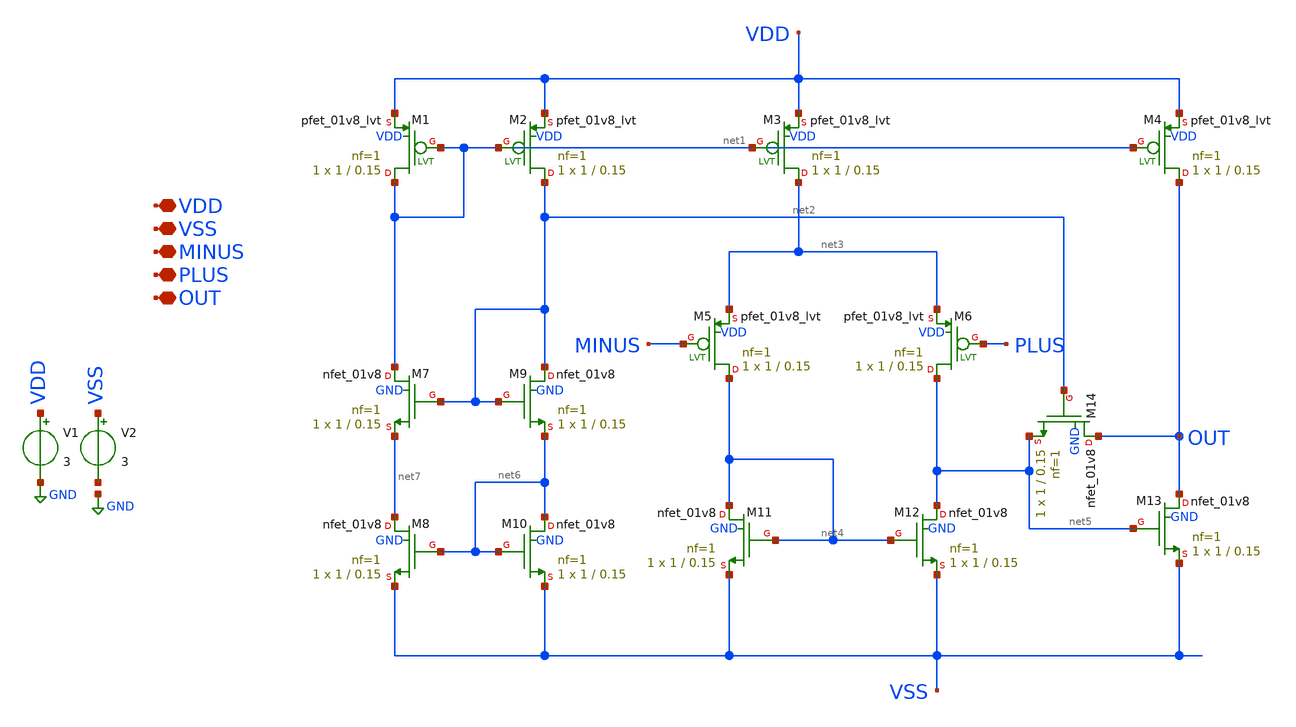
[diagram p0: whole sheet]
** sch_path: peak_two/peak_two.sch
**.subckt peak_two VDD VSS MINUS PLUS OUT
*.iopin VDD
*.iopin VSS
*.iopin MINUS
*.iopin PLUS
*.iopin OUT
XM1 net1 net1 VDD VDD sky130_fd_pr__pfet_01v8_lvt L=0.15 W=1 nf=1 ad='int((nf+1)/2) * W/nf * 0.29' as='int((nf+2)/2) * W/nf * 0.29'
+ pd='2*int((nf+1)/2) * (W/nf + 0.29)' ps='2*int((nf+2)/2) * (W/nf + 0.29)' nrd='0.29 / W' nrs='0.29 / W'
+ sa=0 sb=0 sd=0 mult=1 m=1
XM2 net2 net1 VDD VDD sky130_fd_pr__pfet_01v8_lvt L=0.15 W=1 nf=1 ad='int((nf+1)/2) * W/nf * 0.29' as='int((nf+2)/2) * W/nf * 0.29'
+ pd='2*int((nf+1)/2) * (W/nf + 0.29)' ps='2*int((nf+2)/2) * (W/nf + 0.29)' nrd='0.29 / W' nrs='0.29 / W'
+ sa=0 sb=0 sd=0 mult=1 m=1
XM3 net3 net1 VDD VDD sky130_fd_pr__pfet_01v8_lvt L=0.15 W=1 nf=1 ad='int((nf+1)/2) * W/nf * 0.29' as='int((nf+2)/2) * W/nf * 0.29'
+ pd='2*int((nf+1)/2) * (W/nf + 0.29)' ps='2*int((nf+2)/2) * (W/nf + 0.29)' nrd='0.29 / W' nrs='0.29 / W'
+ sa=0 sb=0 sd=0 mult=1 m=1
XM4 OUT net1 VDD VDD sky130_fd_pr__pfet_01v8_lvt L=0.15 W=1 nf=1 ad='int((nf+1)/2) * W/nf * 0.29' as='int((nf+2)/2) * W/nf * 0.29'
+ pd='2*int((nf+1)/2) * (W/nf + 0.29)' ps='2*int((nf+2)/2) * (W/nf + 0.29)' nrd='0.29 / W' nrs='0.29 / W'
+ sa=0 sb=0 sd=0 mult=1 m=1
XM5 net4 MINUS net3 VDD sky130_fd_pr__pfet_01v8_lvt L=0.15 W=1 nf=1 ad='int((nf+1)/2) * W/nf * 0.29'
+ as='int((nf+2)/2) * W/nf * 0.29' pd='2*int((nf+1)/2) * (W/nf + 0.29)' ps='2*int((nf+2)/2) * (W/nf + 0.29)'
+ nrd='0.29 / W' nrs='0.29 / W' sa=0 sb=0 sd=0 mult=1 m=1
XM6 net5 PLUS net3 VDD sky130_fd_pr__pfet_01v8_lvt L=0.15 W=1 nf=1 ad='int((nf+1)/2) * W/nf * 0.29' as='int((nf+2)/2) * W/nf * 0.29'
+ pd='2*int((nf+1)/2) * (W/nf + 0.29)' ps='2*int((nf+2)/2) * (W/nf + 0.29)' nrd='0.29 / W' nrs='0.29 / W'
+ sa=0 sb=0 sd=0 mult=1 m=1
XM9 net2 net2 net6 GND sky130_fd_pr__nfet_01v8 L=0.15 W=1 nf=1 ad='int((nf+1)/2) * W/nf * 0.29' as='int((nf+2)/2) * W/nf * 0.29'
+ pd='2*int((nf+1)/2) * (W/nf + 0.29)' ps='2*int((nf+2)/2) * (W/nf + 0.29)' nrd='0.29 / W' nrs='0.29 / W'
+ sa=0 sb=0 sd=0 mult=1 m=1
XM7 net1 net2 net7 GND sky130_fd_pr__nfet_01v8 L=0.15 W=1 nf=1 ad='int((nf+1)/2) * W/nf * 0.29' as='int((nf+2)/2) * W/nf * 0.29'
+ pd='2*int((nf+1)/2) * (W/nf + 0.29)' ps='2*int((nf+2)/2) * (W/nf + 0.29)' nrd='0.29 / W' nrs='0.29 / W'
+ sa=0 sb=0 sd=0 mult=1 m=1
XM8 net7 net6 VSS GND sky130_fd_pr__nfet_01v8 L=0.15 W=1 nf=1 ad='int((nf+1)/2) * W/nf * 0.29' as='int((nf+2)/2) * W/nf * 0.29'
+ pd='2*int((nf+1)/2) * (W/nf + 0.29)' ps='2*int((nf+2)/2) * (W/nf + 0.29)' nrd='0.29 / W' nrs='0.29 / W'
+ sa=0 sb=0 sd=0 mult=1 m=1
XM10 net6 net6 VSS GND sky130_fd_pr__nfet_01v8 L=0.15 W=1 nf=1 ad='int((nf+1)/2) * W/nf * 0.29' as='int((nf+2)/2) * W/nf * 0.29'
+ pd='2*int((nf+1)/2) * (W/nf + 0.29)' ps='2*int((nf+2)/2) * (W/nf + 0.29)' nrd='0.29 / W' nrs='0.29 / W'
+ sa=0 sb=0 sd=0 mult=1 m=1
XM11 net4 net4 VSS GND sky130_fd_pr__nfet_01v8 L=0.15 W=1 nf=1 ad='int((nf+1)/2) * W/nf * 0.29' as='int((nf+2)/2) * W/nf * 0.29'
+ pd='2*int((nf+1)/2) * (W/nf + 0.29)' ps='2*int((nf+2)/2) * (W/nf + 0.29)' nrd='0.29 / W' nrs='0.29 / W'
+ sa=0 sb=0 sd=0 mult=1 m=1
XM12 net5 net4 VSS GND sky130_fd_pr__nfet_01v8 L=0.15 W=1 nf=1 ad='int((nf+1)/2) * W/nf * 0.29' as='int((nf+2)/2) * W/nf * 0.29'
+ pd='2*int((nf+1)/2) * (W/nf + 0.29)' ps='2*int((nf+2)/2) * (W/nf + 0.29)' nrd='0.29 / W' nrs='0.29 / W'
+ sa=0 sb=0 sd=0 mult=1 m=1
XM13 OUT net5 VSS GND sky130_fd_pr__nfet_01v8 L=0.15 W=1 nf=1 ad='int((nf+1)/2) * W/nf * 0.29' as='int((nf+2)/2) * W/nf * 0.29'
+ pd='2*int((nf+1)/2) * (W/nf + 0.29)' ps='2*int((nf+2)/2) * (W/nf + 0.29)' nrd='0.29 / W' nrs='0.29 / W'
+ sa=0 sb=0 sd=0 mult=1 m=1
XM14 OUT net2 net5 GND sky130_fd_pr__nfet_01v8 L=0.15 W=1 nf=1 ad='int((nf+1)/2) * W/nf * 0.29' as='int((nf+2)/2) * W/nf * 0.29'
+ pd='2*int((nf+1)/2) * (W/nf + 0.29)' ps='2*int((nf+2)/2) * (W/nf + 0.29)' nrd='0.29 / W' nrs='0.29 / W'
+ sa=0 sb=0 sd=0 mult=1 m=1
V1 VDD GND 3
V2 VSS net8 3
**.ends
.GLOBAL GND
.end
